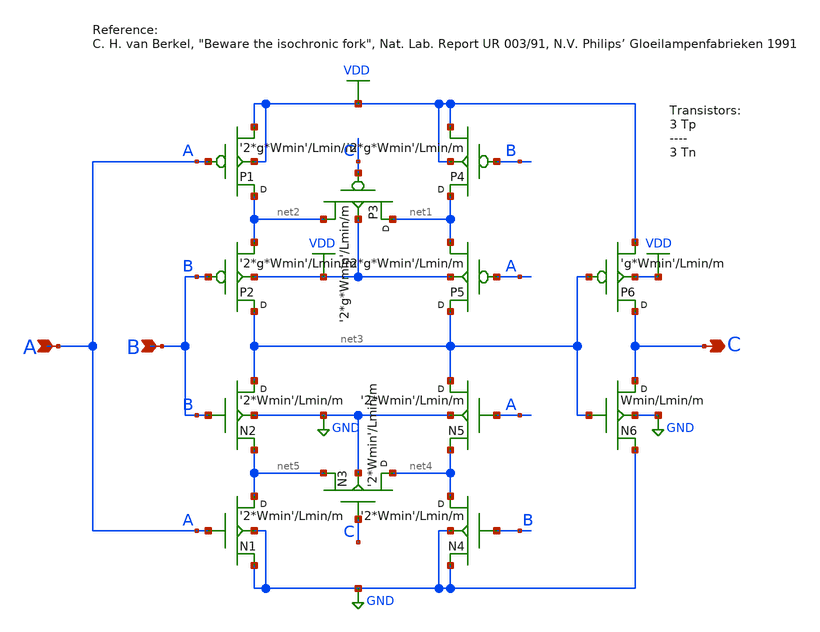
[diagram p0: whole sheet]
** sch_path: Sources/schematics/vanberkel1991.sch
**.subckt vanberkel1991 B C A
*.ipin B
*.opin C
*.ipin A
N2 net3 B net5 GND nmos w='2*Wmin' l=Lmin m=m
P1 net2 A VDD VDD pmos w='2*g*Wmin' l=Lmin m=m
P2 net3 B net2 VDD pmos w='2*g*Wmin' l=Lmin m=m
P4 net1 B VDD VDD pmos w='2*g*Wmin' l=Lmin m=m
P5 net3 A net1 VDD pmos w='2*g*Wmin' l=Lmin m=m
P6 C net3 VDD VDD pmos w='g*Wmin' l=Lmin m=m
N5 net3 A net4 GND nmos w='2*Wmin' l=Lmin m=m
N1 net5 A GND GND nmos w='2*Wmin' l=Lmin m=m
N4 net4 B GND GND nmos w='2*Wmin' l=Lmin m=m
N3 net4 C net5 GND nmos w='2*Wmin' l=Lmin m=m
N6 C net3 GND GND nmos w=Wmin l=Lmin m=m
P3 net1 C net2 VDD pmos w='2*g*Wmin' l=Lmin m=m
**.ends
.GLOBAL GND
.GLOBAL VDD
.end
